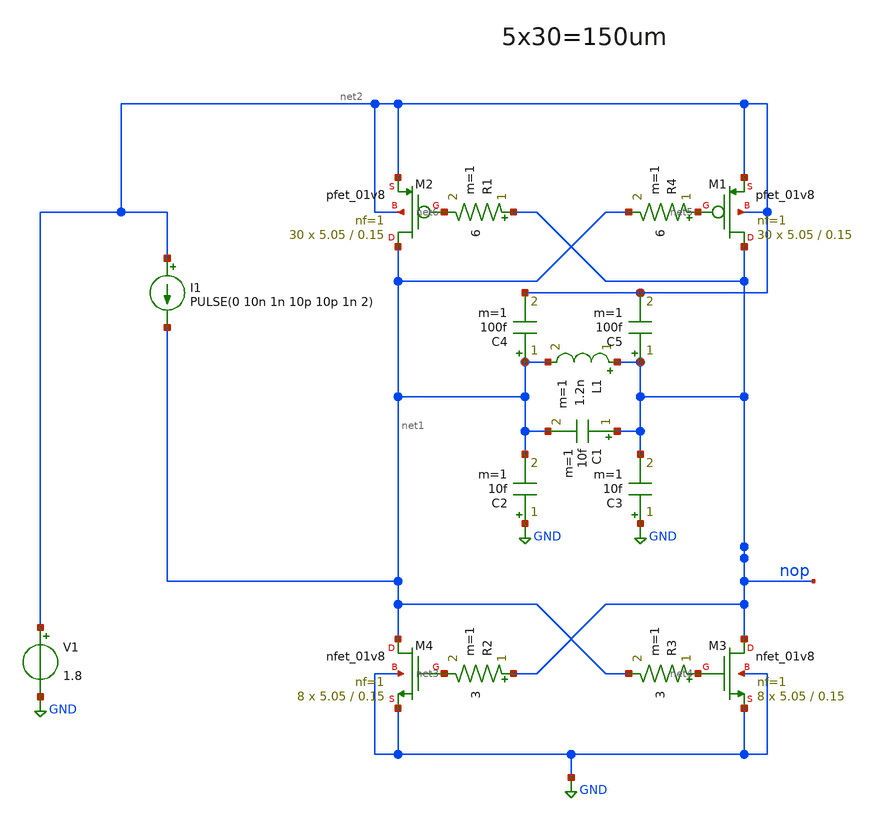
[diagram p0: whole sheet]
** sch_path: xschem/OSC_LF1.sch
**.subckt OSC_LF1
V1 net2 GND 1.8
I1 net2 net1 PULSE(0 10n 1n 10p 10p 1n 2)
R2 nop net3 3 m=1
R3 net4 net1 3 m=1
C1 nop net1 10f m=1
C2 GND net1 10f m=1
C3 GND nop 10f m=1
L1 nop net1 1.2n m=1
XM1 nop net5 net2 net2 sky130_fd_pr__pfet_01v8 L=0.15 W=5.05 nf=1 ad='int((nf+1)/2) * W/nf * 0.29' as='int((nf+2)/2) * W/nf * 0.29'
+ pd='2*int((nf+1)/2) * (W/nf + 0.29)' ps='2*int((nf+2)/2) * (W/nf + 0.29)' nrd='0.29 / W' nrs='0.29 / W'
+ sa=0 sb=0 sd=0 mult=30 m=30
XM2 net1 net6 net2 net2 sky130_fd_pr__pfet_01v8 L=0.15 W=5.05 nf=1 ad='int((nf+1)/2) * W/nf * 0.29' as='int((nf+2)/2) * W/nf * 0.29'
+ pd='2*int((nf+1)/2) * (W/nf + 0.29)' ps='2*int((nf+2)/2) * (W/nf + 0.29)' nrd='0.29 / W' nrs='0.29 / W'
+ sa=0 sb=0 sd=0 mult=30 m=30
R1 nop net6 6 m=1
R4 net5 net1 6 m=1
C4 net1 net2 100f m=1
C5 nop net2 100f m=1
XM3 nop net4 GND GND sky130_fd_pr__nfet_01v8 L=0.15 W=5.05 nf=1 ad='int((nf+1)/2) * W/nf * 0.29' as='int((nf+2)/2) * W/nf * 0.29'
+ pd='2*int((nf+1)/2) * (W/nf + 0.29)' ps='2*int((nf+2)/2) * (W/nf + 0.29)' nrd='0.29 / W' nrs='0.29 / W'
+ sa=0 sb=0 sd=0 mult=8 m=8
XM4 net1 net3 GND GND sky130_fd_pr__nfet_01v8 L=0.15 W=5.05 nf=1 ad='int((nf+1)/2) * W/nf * 0.29' as='int((nf+2)/2) * W/nf * 0.29'
+ pd='2*int((nf+1)/2) * (W/nf + 0.29)' ps='2*int((nf+2)/2) * (W/nf + 0.29)' nrd='0.29 / W' nrs='0.29 / W'
+ sa=0 sb=0 sd=0 mult=8 m=8
**** begin user architecture code
.lib $::SKYWATER_MODELS/sky130.lib.spice ff
* .include $::PDKPATH/libs.ref/sky130_fd_sc_hvl/spice/sky130_fd_sc_hvl.spice



.subckt sky130_fd_pr__rf_nfet_01v8_bM04W5p00L0p15_ext DRAIN GATE SOURCE SUBSTRATE
X0 DRAIN GATE SOURCE SUBSTRATE sky130_fd_pr__nfet_01v8 ad=2.828e+12p pd=2.132e+07u as=4.242e+12p
+ ps=3.198e+07u w=5.05e+06u l=150000u
X1 SOURCE SUBSTRATE SUBSTRATE SUBSTRATE sky130_fd_pr__nfet_01v8 ad=0p pd=0u as=3.03e+12p
+ ps=2.14e+07u w=5.05e+06u l=150000u
X2 SOURCE GATE DRAIN SUBSTRATE sky130_fd_pr__nfet_01v8 ad=0p pd=0u as=0p ps=0u w=5.05e+06u l=150000u
X3 DRAIN GATE SOURCE SUBSTRATE sky130_fd_pr__nfet_01v8 ad=0p pd=0u as=0p ps=0u w=5.05e+06u l=150000u
X4 SUBSTRATE SUBSTRATE SOURCE SUBSTRATE sky130_fd_pr__nfet_01v8 ad=0p pd=0u as=0p ps=0u w=5.05e+06u
+ l=150000u
X5 SOURCE GATE DRAIN SUBSTRATE sky130_fd_pr__nfet_01v8 ad=0p pd=0u as=0p ps=0u w=5.05e+06u l=150000u
.ends
.options savecurrents
.tran 1ps 20ns
.control
run
display
plot v(nop)
plot v(nmid)
plot @I1[i]
.endc


**** end user architecture code
**.ends
.GLOBAL GND
.end
